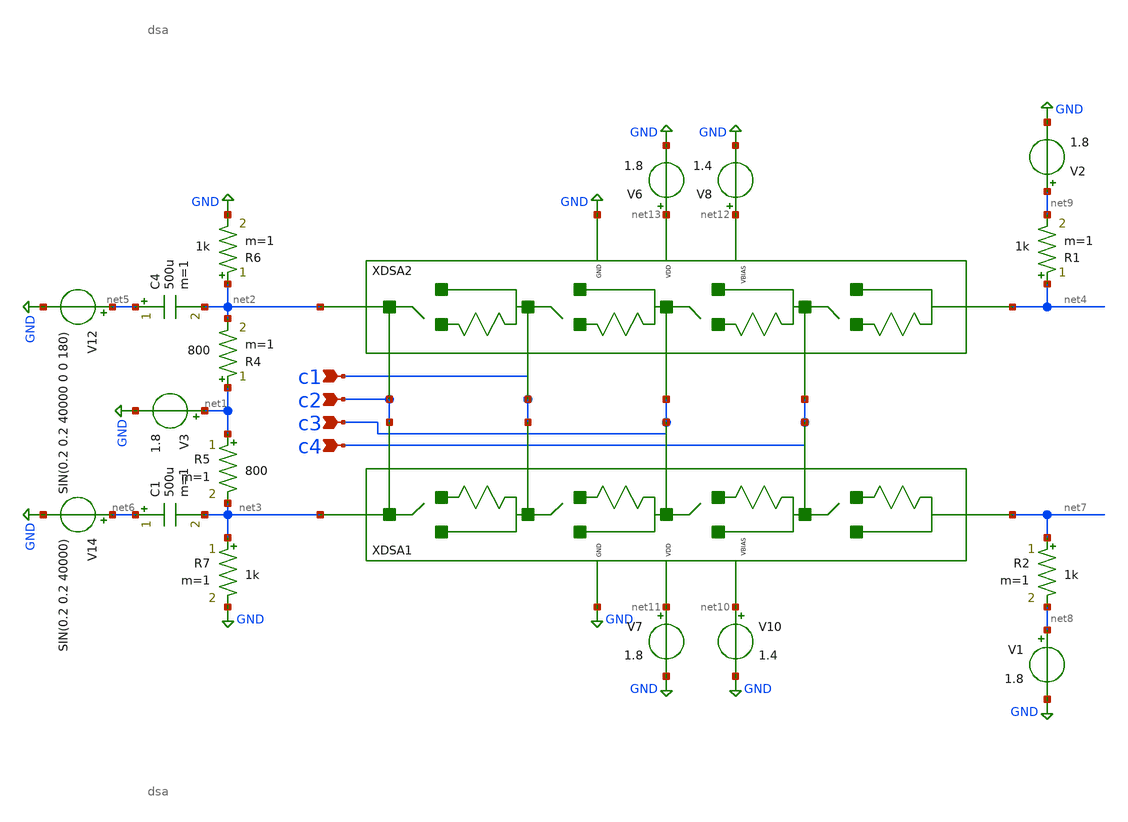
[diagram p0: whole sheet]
** sch_path: xschem/misc/DSA_testbench.sch
**.subckt DSA_testbench c1 c2 c3 c4
*.ipin c1
*.ipin c2
*.ipin c3
*.ipin c4
V3 net1 GND 1.8
R4 net1 net2 800 m=1
R5 net1 net3 800 m=1
R6 net2 GND 1k m=1
R7 net3 GND 1k m=1
XDSA1 net3 c2 c1 c3 c4 net7 net10 net11 GND dsa
XDSA2 net2 c2 c1 c3 c4 net4 net12 net13 GND dsa
V6 net13 GND 1.8
V7 net11 GND 1.8
V8 net12 GND 1.4
V10 net10 GND 1.4
V12 net5 GND SIN(0.2 0.2 40000 0 0 180)
V14 net6 GND SIN(0.2 0.2 40000)
C4 net5 net2 500u m=1
C1 net6 net3 500u m=1
R1 net4 net9 1k m=1
R2 net7 net8 1k m=1
V1 net8 GND 1.8
V2 net9 GND 1.8
**** begin user architecture code


.trans 0.00001s 0.00001s
.save all


 ** manual skywater pdks install (with patches applied)
* .lib $::SKYWATER_MODELS/models/sky130.lib.spice tt
*** remove the /models/

** opencircuitdesign pdks install
.lib /Volumes/WORK_DRIVE/open_pdks/sky130/custom/models/sky130.lib.spice tt

.param mc_mm_switch=0
.param mc_pr_switch=0

**** end user architecture code
**.ends
.GLOBAL GND
.end
